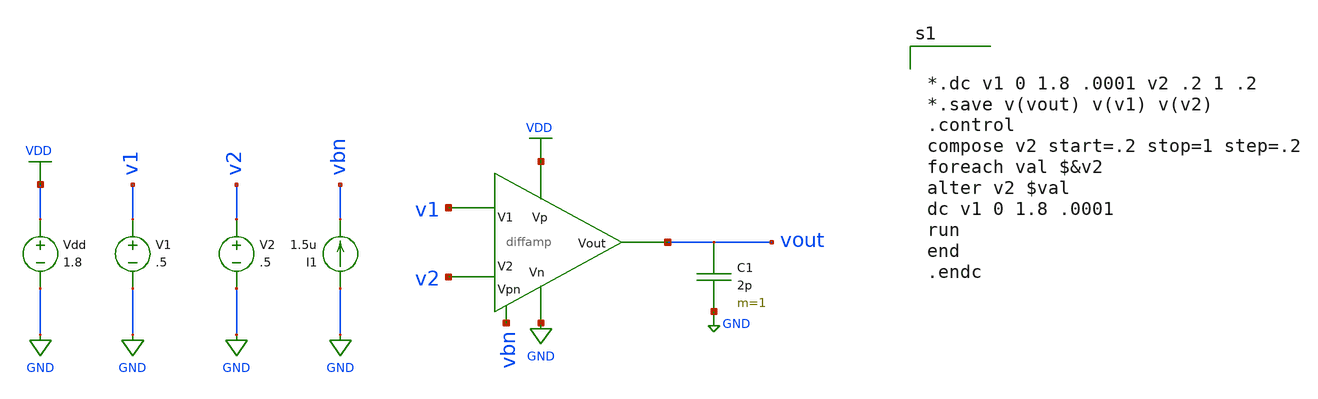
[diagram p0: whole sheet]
** sch_path: mini_proj_3/schematic/diff_2a.sch
**.subckt diff_2a
Vdd VDD GND 1.8
V1 v1 GND .5
V2 v2 GND .5
I1 GND vbn 1.5u
C1 vout GND 2p m=1
X1 vbn VDD GND v1 v2 vout diffamp
**** begin user architecture code

.option wnflag=1
.lib ~/skywater/skywater-pdk/libraries/sky130_fd_pr_ngspice/latest/models/sky130.lib.spice tt



*.dc v1 0 1.8 .0001 v2 .2 1 .2
*.save v(vout) v(v1) v(v2)
.control
compose v2 start=.2 stop=1 step=.2
foreach val $&v2
alter v2 $val
dc v1 0 1.8 .0001
run
end
.endc


**** end user architecture code
**.ends
.GLOBAL VDD
.GLOBAL GND
.end
